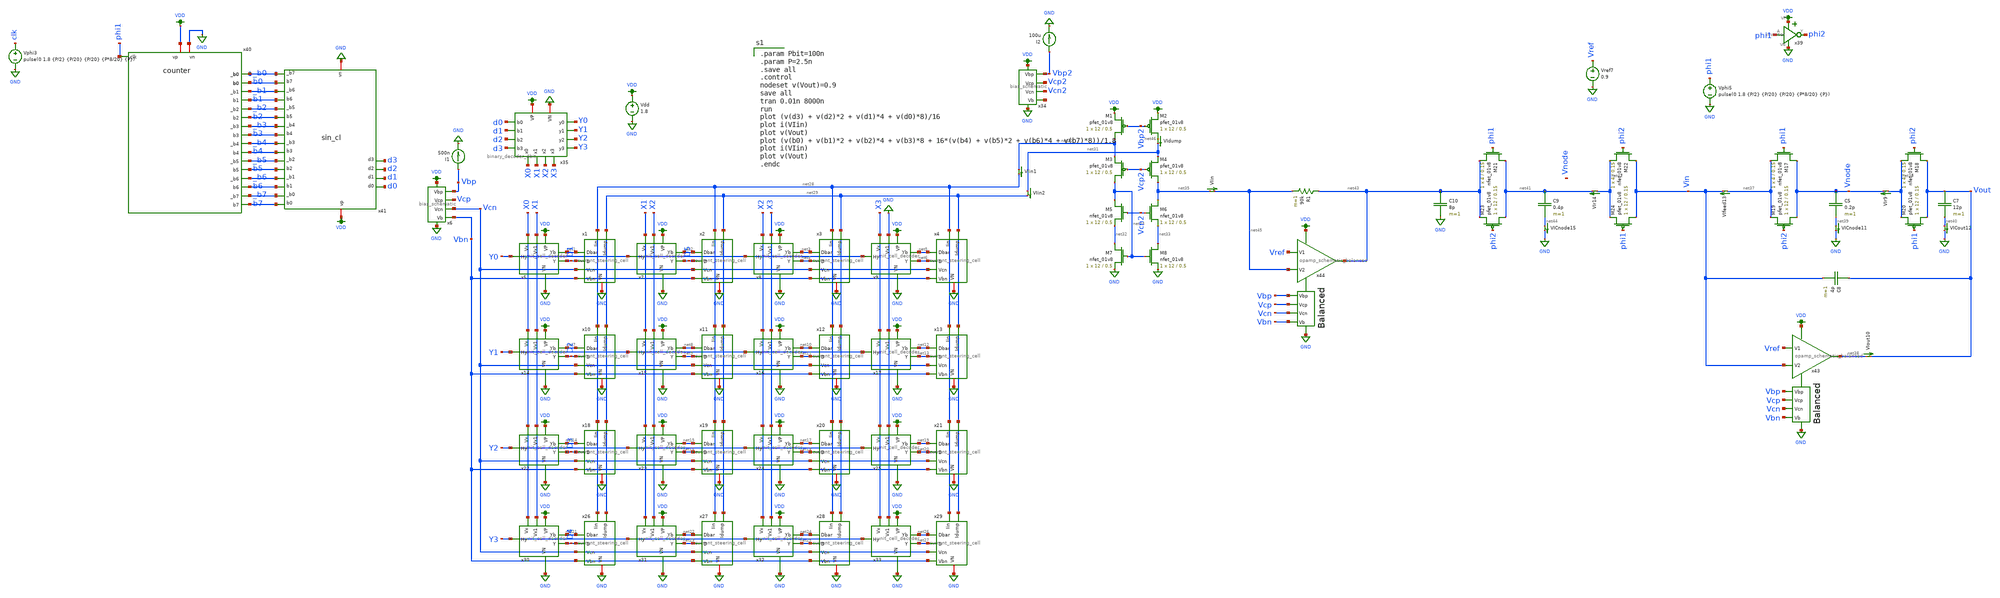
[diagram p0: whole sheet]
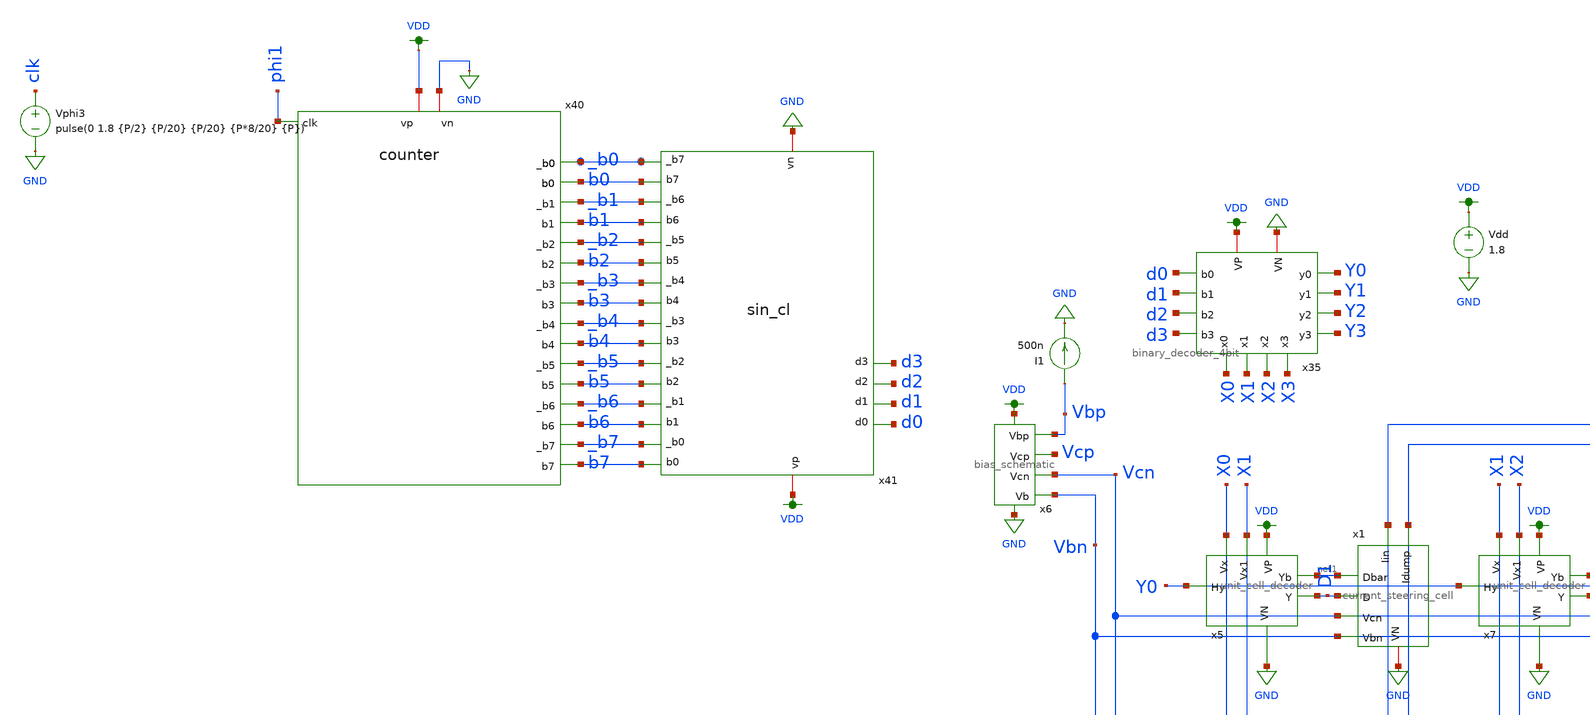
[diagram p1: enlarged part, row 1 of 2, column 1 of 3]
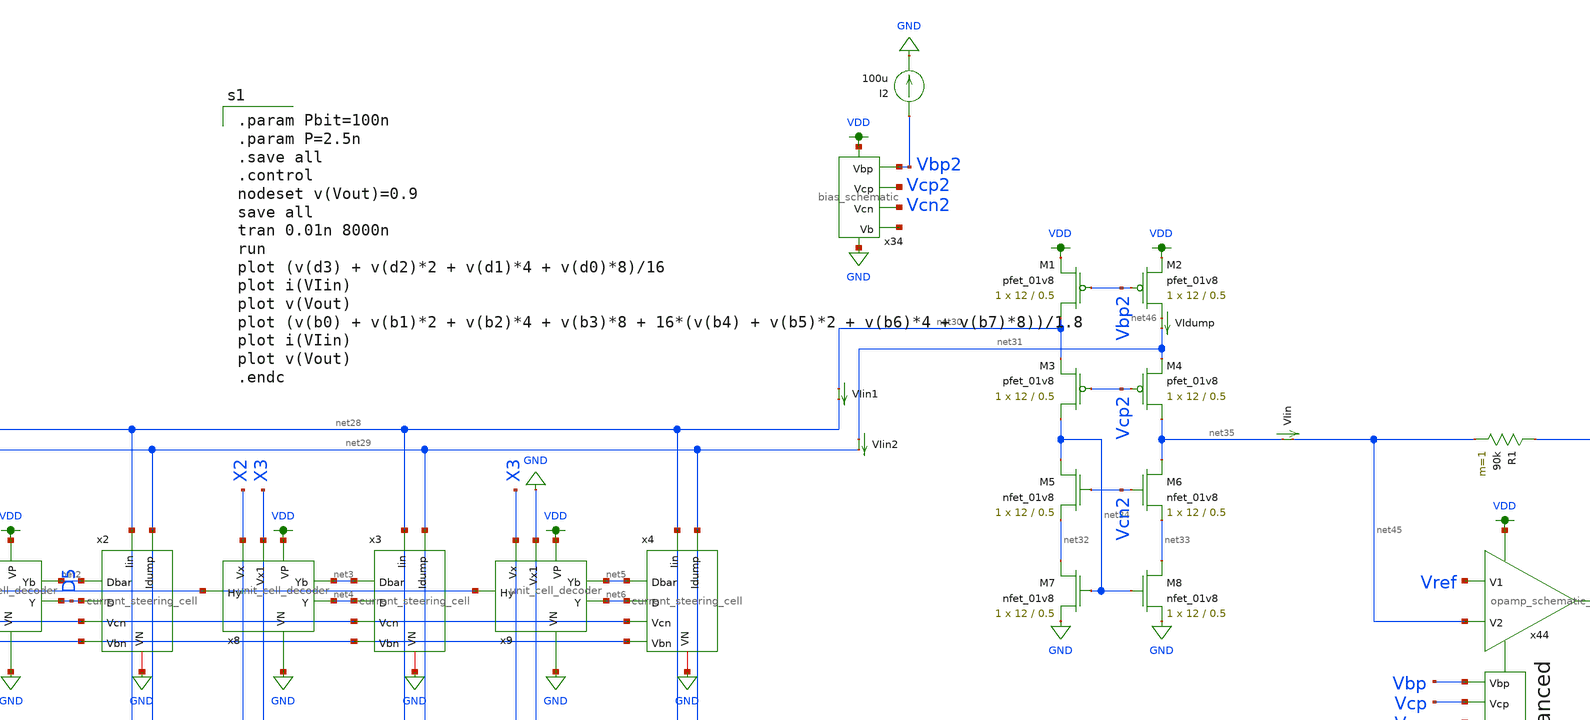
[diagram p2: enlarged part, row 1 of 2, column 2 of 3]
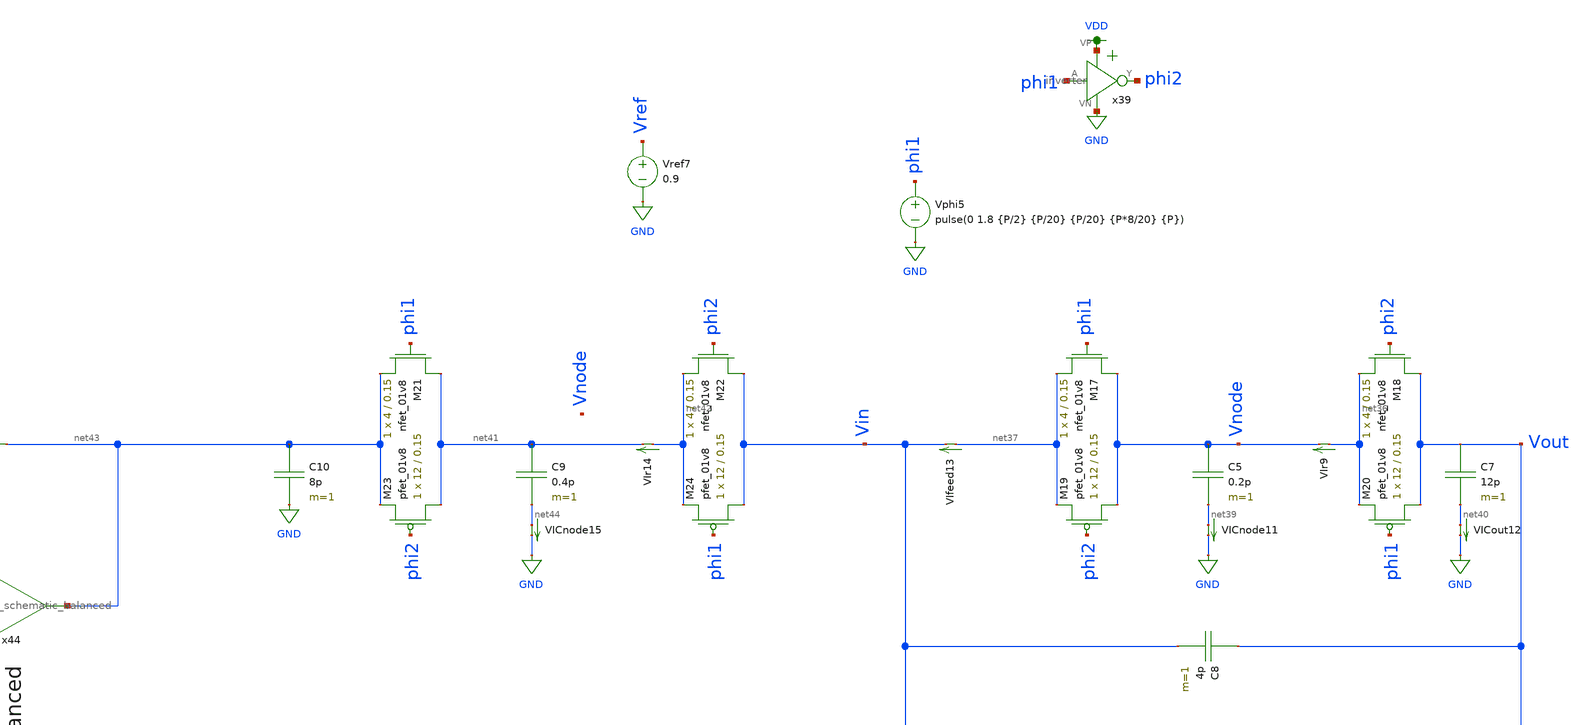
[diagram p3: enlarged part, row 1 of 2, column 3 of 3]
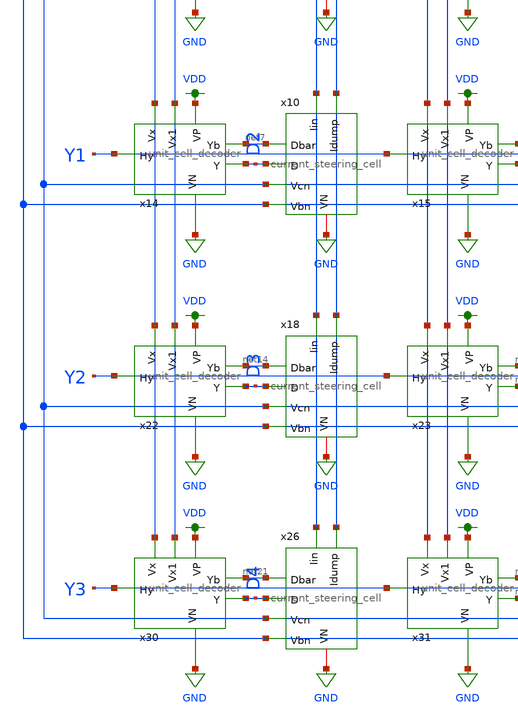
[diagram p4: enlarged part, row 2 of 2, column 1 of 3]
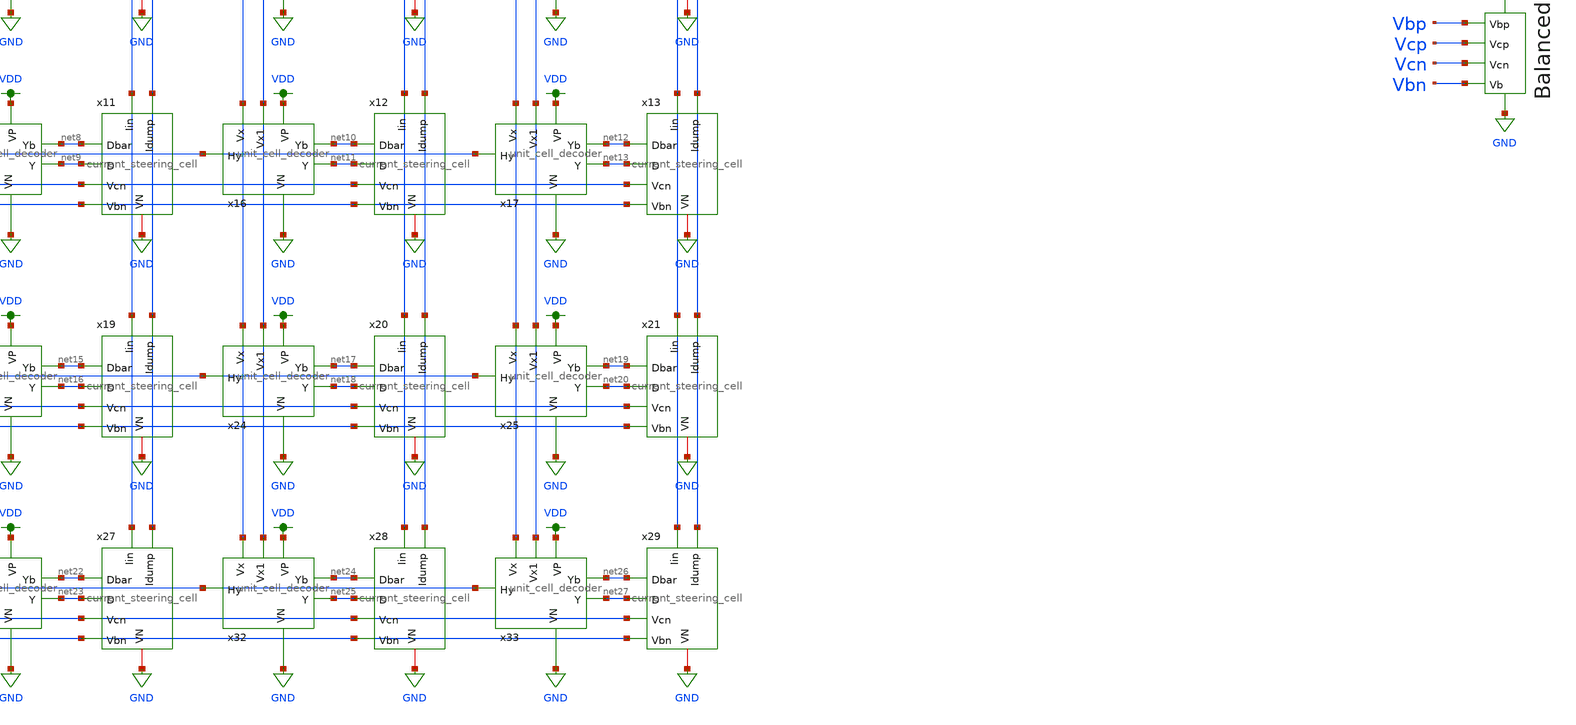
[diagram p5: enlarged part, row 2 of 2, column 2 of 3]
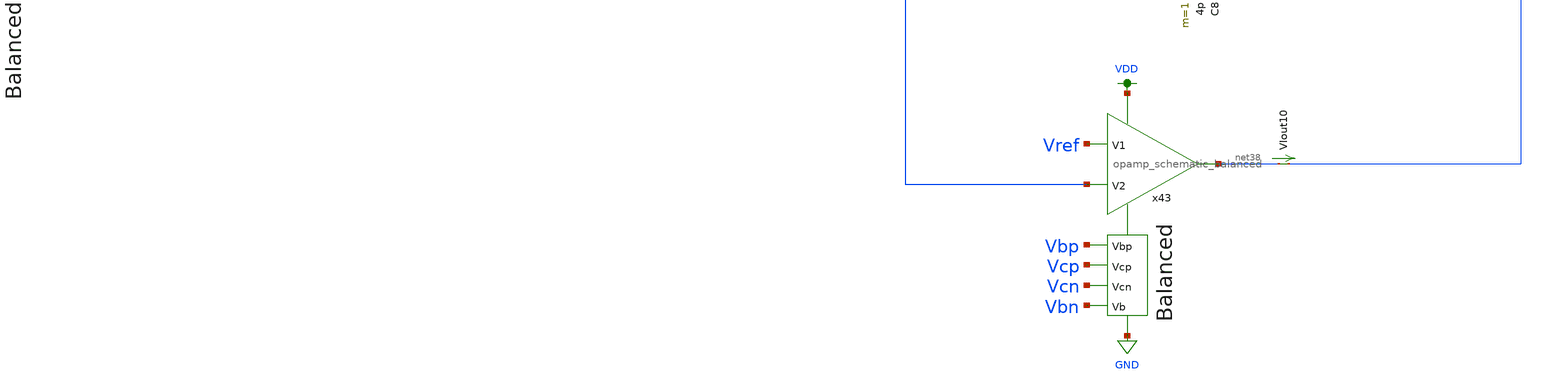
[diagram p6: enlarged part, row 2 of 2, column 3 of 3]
** sch_path: xschem/current_steering_testbenches/current_steering_testbench_transient_full1.sch
**.subckt current_steering_testbench_transient_full1
I1 Vbp GND 500n
VIin net35 net45 0
.save i(viin)
Vdd VDD GND 1.8
XM1 net30 Vbp2 VDD VDD sky130_fd_pr__pfet_01v8 L=0.5 W=12 nf=1 ad='int((nf+1)/2) * W/nf * 0.29' as='int((nf+2)/2) * W/nf * 0.29'
+ pd='2*int((nf+1)/2) * (W/nf + 0.29)' ps='2*int((nf+2)/2) * (W/nf + 0.29)' nrd='0.29 / W' nrs='0.29 / W'
+ sa=0 sb=0 sd=0 mult=1 m=1
XM2 net46 Vbp2 VDD VDD sky130_fd_pr__pfet_01v8 L=0.5 W=12 nf=1 ad='int((nf+1)/2) * W/nf * 0.29' as='int((nf+2)/2) * W/nf * 0.29'
+ pd='2*int((nf+1)/2) * (W/nf + 0.29)' ps='2*int((nf+2)/2) * (W/nf + 0.29)' nrd='0.29 / W' nrs='0.29 / W'
+ sa=0 sb=0 sd=0 mult=1 m=1
XM3 net34 Vcp2 net30 VDD sky130_fd_pr__pfet_01v8 L=0.5 W=12 nf=1 ad='int((nf+1)/2) * W/nf * 0.29' as='int((nf+2)/2) * W/nf * 0.29'
+ pd='2*int((nf+1)/2) * (W/nf + 0.29)' ps='2*int((nf+2)/2) * (W/nf + 0.29)' nrd='0.29 / W' nrs='0.29 / W'
+ sa=0 sb=0 sd=0 mult=1 m=1
XM4 net35 Vcp2 net31 VDD sky130_fd_pr__pfet_01v8 L=0.5 W=12 nf=1 ad='int((nf+1)/2) * W/nf * 0.29' as='int((nf+2)/2) * W/nf * 0.29'
+ pd='2*int((nf+1)/2) * (W/nf + 0.29)' ps='2*int((nf+2)/2) * (W/nf + 0.29)' nrd='0.29 / W' nrs='0.29 / W'
+ sa=0 sb=0 sd=0 mult=1 m=1
x5 X0 X1 Y0 VDD GND net1 D1 unit_cell_decoder
x7 X1 X2 Y0 VDD GND net2 D5 unit_cell_decoder
x8 X2 X3 Y0 VDD GND net3 net4 unit_cell_decoder
x9 X3 GND Y0 VDD GND net5 net6 unit_cell_decoder
x14 X0 X1 Y1 VDD GND net7 D2 unit_cell_decoder
x15 X1 X2 Y1 VDD GND net8 net9 unit_cell_decoder
x16 X2 X3 Y1 VDD GND net10 net11 unit_cell_decoder
x17 X3 GND Y1 VDD GND net12 net13 unit_cell_decoder
x22 X0 X1 Y2 VDD GND net14 D3 unit_cell_decoder
x23 X1 X2 Y2 VDD GND net15 net16 unit_cell_decoder
x24 X2 X3 Y2 VDD GND net17 net18 unit_cell_decoder
x25 X3 GND Y2 VDD GND net19 net20 unit_cell_decoder
x30 X0 X1 Y3 VDD GND net21 D4 unit_cell_decoder
x31 X1 X2 Y3 VDD GND net22 net23 unit_cell_decoder
x32 X2 X3 Y3 VDD GND net24 net25 unit_cell_decoder
x33 X3 GND Y3 VDD GND net26 net27 unit_cell_decoder
x1 net28 net29 net1 D1 Vcn Vbn GND current_steering_cell
x2 net28 net29 net2 D5 Vcn Vbn GND current_steering_cell
x3 net28 net29 net3 net4 Vcn Vbn GND current_steering_cell
x4 net28 net29 net5 net6 Vcn Vbn GND current_steering_cell
x10 net28 net29 net7 D2 Vcn Vbn GND current_steering_cell
x11 net28 net29 net8 net9 Vcn Vbn GND current_steering_cell
x12 net28 net29 net10 net11 Vcn Vbn GND current_steering_cell
x13 net28 net29 net12 net13 Vcn Vbn GND current_steering_cell
x18 net28 net29 net14 D3 Vcn Vbn GND current_steering_cell
x19 net28 net29 net15 net16 Vcn Vbn GND current_steering_cell
x20 net28 net29 net17 net18 Vcn Vbn GND current_steering_cell
x21 net28 net29 net19 net20 Vcn Vbn GND current_steering_cell
x26 net28 net29 net21 D4 Vcn Vbn GND current_steering_cell
x27 net28 net29 net22 net23 Vcn Vbn GND current_steering_cell
x28 net28 net29 net24 net25 Vcn Vbn GND current_steering_cell
x29 net28 net29 net26 net27 Vcn Vbn GND current_steering_cell
x6 VDD Vbp Vcp Vcn GND Vbn bias_schematic
XM5 net34 Vcn2 net32 GND sky130_fd_pr__nfet_01v8 L=0.5 W=12 nf=1 ad='int((nf+1)/2) * W/nf * 0.29' as='int((nf+2)/2) * W/nf * 0.29'
+ pd='2*int((nf+1)/2) * (W/nf + 0.29)' ps='2*int((nf+2)/2) * (W/nf + 0.29)' nrd='0.29 / W' nrs='0.29 / W'
+ sa=0 sb=0 sd=0 mult=1 m=1
XM6 net35 Vcn2 net33 GND sky130_fd_pr__nfet_01v8 L=0.5 W=12 nf=1 ad='int((nf+1)/2) * W/nf * 0.29' as='int((nf+2)/2) * W/nf * 0.29'
+ pd='2*int((nf+1)/2) * (W/nf + 0.29)' ps='2*int((nf+2)/2) * (W/nf + 0.29)' nrd='0.29 / W' nrs='0.29 / W'
+ sa=0 sb=0 sd=0 mult=1 m=1
XM7 net32 net34 GND GND sky130_fd_pr__nfet_01v8 L=0.5 W=12 nf=1 ad='int((nf+1)/2) * W/nf * 0.29' as='int((nf+2)/2) * W/nf * 0.29'
+ pd='2*int((nf+1)/2) * (W/nf + 0.29)' ps='2*int((nf+2)/2) * (W/nf + 0.29)' nrd='0.29 / W' nrs='0.29 / W'
+ sa=0 sb=0 sd=0 mult=1 m=1
XM8 net33 net34 GND GND sky130_fd_pr__nfet_01v8 L=0.5 W=12 nf=1 ad='int((nf+1)/2) * W/nf * 0.29' as='int((nf+2)/2) * W/nf * 0.29'
+ pd='2*int((nf+1)/2) * (W/nf + 0.29)' ps='2*int((nf+2)/2) * (W/nf + 0.29)' nrd='0.29 / W' nrs='0.29 / W'
+ sa=0 sb=0 sd=0 mult=1 m=1
VIdump net46 net31 0
.save i(vidump)
I2 Vbp2 GND 100u
x34 VDD Vbp2 Vcp2 Vcn2 GND net47 bias_schematic
x35 Y0 X0 X1 Y1 VDD d0 d1 X2 Y2 d2 d3 GND Y3 X3 binary_decoder_4bit
x40 VDD GND phi1 _b1 b1 _b2 b2 _b3 b3 _b0 b0 _b5 b5 _b6 b6 _b7 b7 _b4 b4 counter
x41 b6 _b6 b5 _b5 b4 _b4 b3 VDD _b3 GND b2 _b2 b1 _b1 d0 b7 b0 _b7 _b0 d1 d2 d3 sin_cl
Vphi3 clk GND pulse(0 1.8 {P/2} {P/20} {P/20} {P*8/20} {P})
C5 Vnode net39 0.2p m=1
XM17 Vnode phi1 net37 GND sky130_fd_pr__nfet_01v8 L=0.15 W=4 nf=1 ad='int((nf+1)/2) * W/nf * 0.29' as='int((nf+2)/2) * W/nf * 0.29'
+ pd='2*int((nf+1)/2) * (W/nf + 0.29)' ps='2*int((nf+2)/2) * (W/nf + 0.29)' nrd='0.29 / W' nrs='0.29 / W'
+ sa=0 sb=0 sd=0 mult=1 m=1
XM18 Vout phi2 net36 GND sky130_fd_pr__nfet_01v8 L=0.15 W=4 nf=1 ad='int((nf+1)/2) * W/nf * 0.29' as='int((nf+2)/2) * W/nf * 0.29'
+ pd='2*int((nf+1)/2) * (W/nf + 0.29)' ps='2*int((nf+2)/2) * (W/nf + 0.29)' nrd='0.29 / W' nrs='0.29 / W'
+ sa=0 sb=0 sd=0 mult=1 m=1
Vphi5 phi1 GND pulse(0 1.8 {P/2} {P/20} {P/20} {P*8/20} {P})
C7 Vout net40 12p m=1
XM19 Vnode phi2 net37 VDD sky130_fd_pr__pfet_01v8 L=0.15 W=12 nf=1 ad='int((nf+1)/2) * W/nf * 0.29' as='int((nf+2)/2) * W/nf * 0.29'
+ pd='2*int((nf+1)/2) * (W/nf + 0.29)' ps='2*int((nf+2)/2) * (W/nf + 0.29)' nrd='0.29 / W' nrs='0.29 / W'
+ sa=0 sb=0 sd=0 mult=1 m=1
XM20 Vout phi1 net36 VDD sky130_fd_pr__pfet_01v8 L=0.15 W=12 nf=1 ad='int((nf+1)/2) * W/nf * 0.29' as='int((nf+2)/2) * W/nf * 0.29'
+ pd='2*int((nf+1)/2) * (W/nf + 0.29)' ps='2*int((nf+2)/2) * (W/nf + 0.29)' nrd='0.29 / W' nrs='0.29 / W'
+ sa=0 sb=0 sd=0 mult=1 m=1
x39 VDD phi1 phi2 GND inverter
Vref7 Vref GND 0.9
VIr9 net36 Vnode 0
.save i(vir9)
VIout10 net38 Vout 0
.save i(viout10)
VICnode11 net39 GND 0
.save i(vicnode11)
VICout12 net40 GND 0
.save i(vicout12)
VIfeed13 net37 Vin 0
.save i(vifeed13)
C8 Vout Vin 4p m=1
x43 VDD Vbp Vcp net38 Vref Vin Vcn Vbn GND opamp_schematic_balanced
C9 net41 net44 0.4p m=1
XM21 net41 phi1 net43 GND sky130_fd_pr__nfet_01v8 L=0.15 W=4 nf=1 ad='int((nf+1)/2) * W/nf * 0.29' as='int((nf+2)/2) * W/nf * 0.29'
+ pd='2*int((nf+1)/2) * (W/nf + 0.29)' ps='2*int((nf+2)/2) * (W/nf + 0.29)' nrd='0.29 / W' nrs='0.29 / W'
+ sa=0 sb=0 sd=0 mult=1 m=1
XM22 Vin phi2 net42 GND sky130_fd_pr__nfet_01v8 L=0.15 W=4 nf=1 ad='int((nf+1)/2) * W/nf * 0.29' as='int((nf+2)/2) * W/nf * 0.29'
+ pd='2*int((nf+1)/2) * (W/nf + 0.29)' ps='2*int((nf+2)/2) * (W/nf + 0.29)' nrd='0.29 / W' nrs='0.29 / W'
+ sa=0 sb=0 sd=0 mult=1 m=1
XM23 net41 phi2 net43 VDD sky130_fd_pr__pfet_01v8 L=0.15 W=12 nf=1 ad='int((nf+1)/2) * W/nf * 0.29' as='int((nf+2)/2) * W/nf * 0.29'
+ pd='2*int((nf+1)/2) * (W/nf + 0.29)' ps='2*int((nf+2)/2) * (W/nf + 0.29)' nrd='0.29 / W' nrs='0.29 / W'
+ sa=0 sb=0 sd=0 mult=1 m=1
XM24 Vin phi1 net42 VDD sky130_fd_pr__pfet_01v8 L=0.15 W=12 nf=1 ad='int((nf+1)/2) * W/nf * 0.29' as='int((nf+2)/2) * W/nf * 0.29'
+ pd='2*int((nf+1)/2) * (W/nf + 0.29)' ps='2*int((nf+2)/2) * (W/nf + 0.29)' nrd='0.29 / W' nrs='0.29 / W'
+ sa=0 sb=0 sd=0 mult=1 m=1
VIr14 net42 net41 0
.save i(vir14)
VICnode15 net44 GND 0
.save i(vicnode15)
C10 net43 GND 8p m=1
x44 VDD Vbp Vcp net43 Vref net45 Vcn Vbn GND opamp_schematic_balanced
R1 net43 net45 90k m=1
VIin1 net30 net28 0
.save i(viin1)
VIin2 net31 net29 0
.save i(viin2)
**** begin user architecture code

.option wnflag=1
.param MC_SWITCH=0.0
.lib ~/skywater/skywater-pdk/libraries/sky130_fd_pr_ngspice/latest/models/sky130.lib.spice tt


.param Pbit=100n
.param P=2.5n
.save all
.control
nodeset v(Vout)=0.9
save all
tran 0.01n 8000n
run
plot (v(d3) + v(d2)*2 + v(d1)*4 + v(d0)*8)/16
plot i(VIin)
plot v(Vout)
plot (v(b0) + v(b1)*2 + v(b2)*4 + v(b3)*8 + 16*(v(b4) + v(b5)*2 + v(b6)*4 + v(b7)*8))/1.8
plot i(VIin)
plot v(Vout)
.endc

**** end user architecture code
**.ends
.GLOBAL GND
.GLOBAL VDD
.end
